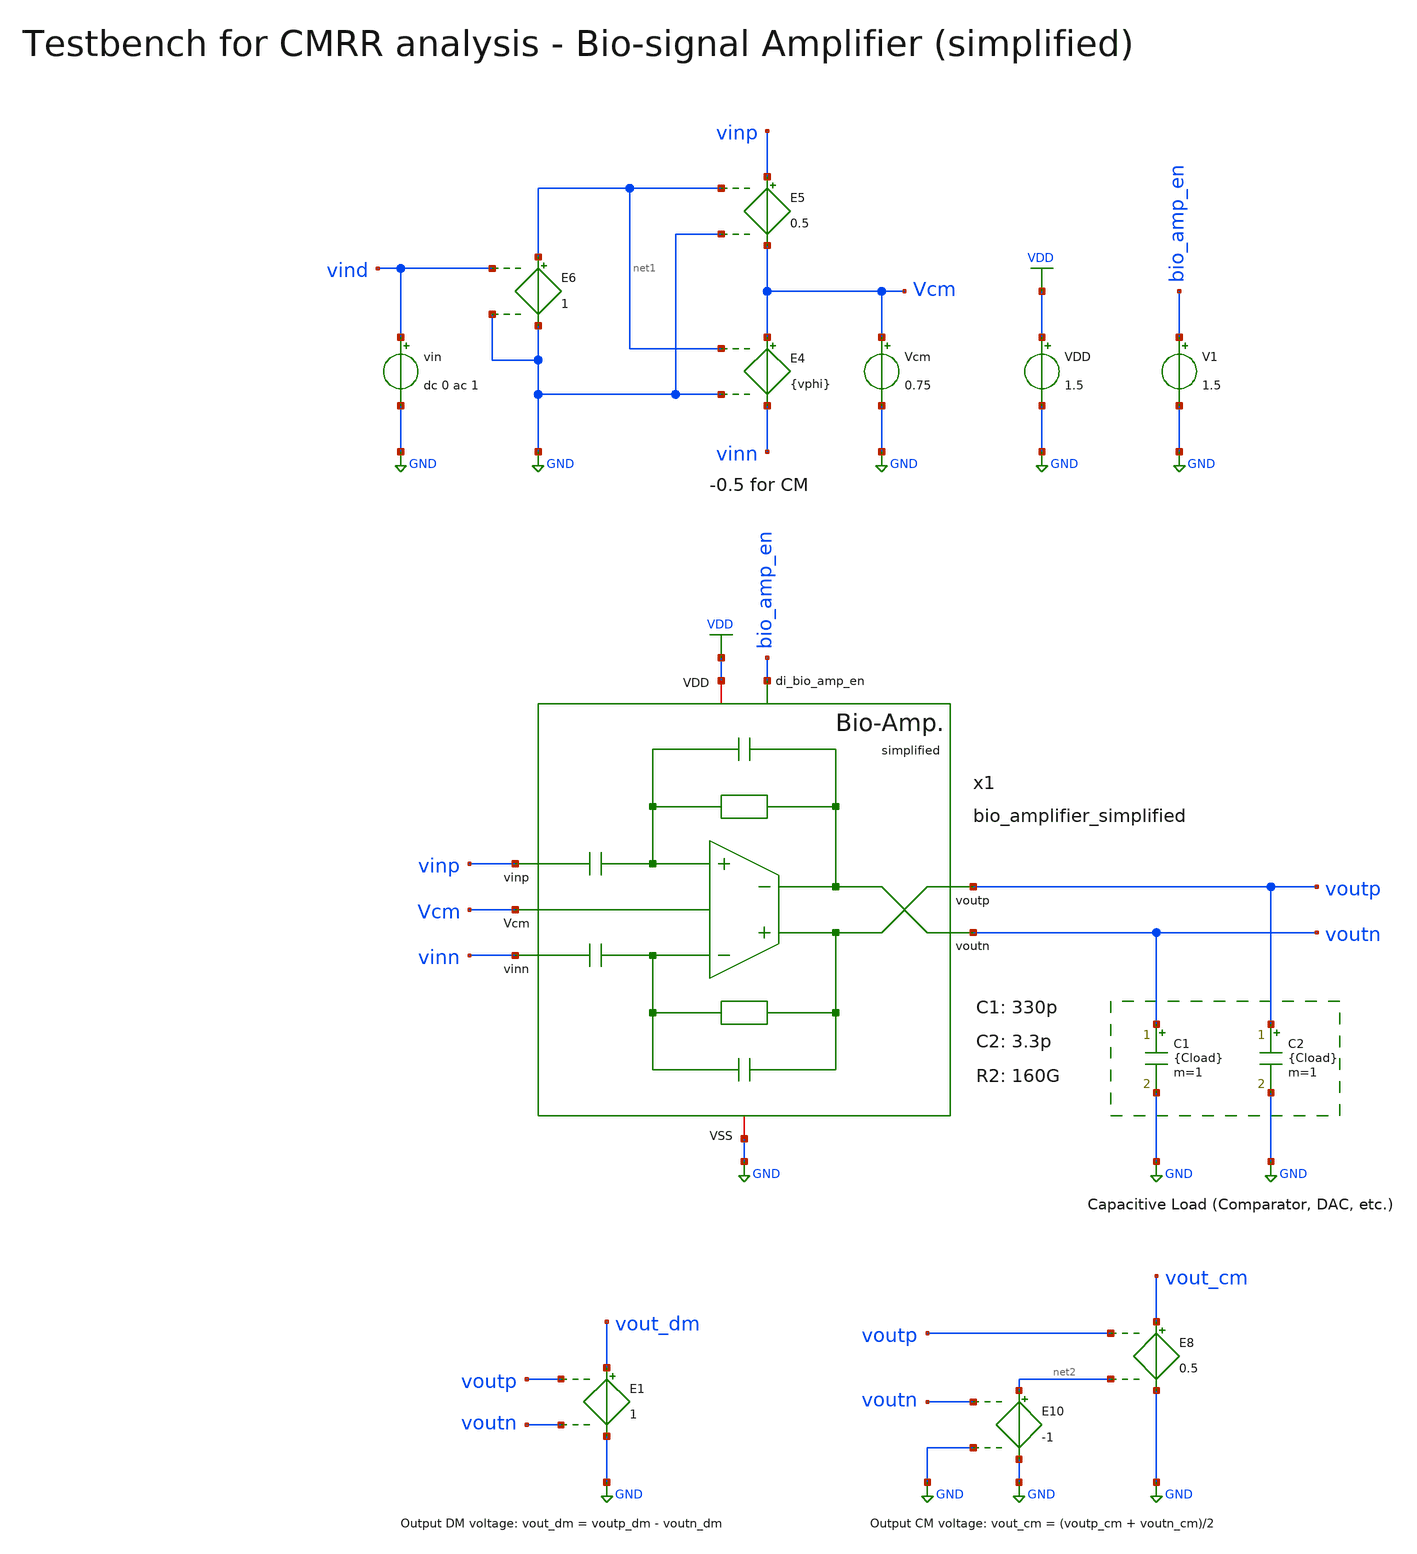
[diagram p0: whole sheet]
** sch_path: SG13G2_ATBS-ADC-main/xschem/bio_amplifier/testbenches/bio_amplifier_simplified_tb_CMRR.sch
**.subckt bio_amplifier_simplified_tb_CMRR
VDD VDD GND 1.5
C1 voutn GND {Cload} m=1
C2 voutp GND {Cload} m=1
Vcm Vcm GND 0.75
E4 Vcm vinn net1 GND {vphi}
E5 vinp Vcm net1 GND 0.5
E6 net1 GND vind GND 1
V1 bio_amp_en GND 1.5
vin vind GND dc 0 ac 1
x1 voutp bio_amp_en vinp Vcm voutn vinn VDD GND bio_amplifier_simplified C1=330p C2=3.3p R2=160G
E1 vout_dm GND voutp voutn 1
E8 vout_cm GND voutp net2 0.5
E10 net2 GND voutn GND -1
**** begin user architecture code

.lib cornerMOSlv.lib mos_tt
.lib cornerMOShv.lib mos_tt
.lib cornerRES.lib res_typ



.param temp=27
* 227.56fF DAC
.param Cload=227.56f
.param vphi=0.5
.param f_min = 10m
.csparam f_min = f_min
.param f_max = 1G
.csparam f_max = f_max
.param fdc = 10
.csparam fdc = fdc
.options savecurrents method=gear reltol=1e-2 abstol=1e-15 gmin=1e-15 rshunt=1e12
.control

* Operating Point Analysis
optran 0 0 0 1u 1m 0
save all
op
remzerovec
write bio_amplifier_simplified_tb_CMRR.raw
set appendwrite
reset

* Differential-Mode
optran 0 0 0 1u 1m 0
save v(vout_dm) v(vind)

* AC Analysis (Differential-Mode)
ac dec 101 $&f_min $&f_max
remzerovec
write bio_amplifier_simplified_tb_CMRR.raw

* Plotting Differential Mode Gain
let Adm = v(vout_dm)/v(vind)
let Adm_dB = vdb(Adm)
let Adm_arg = 180/PI*cphase(Adm)
plot Adm_dB Adm_arg ylabel 'Magnitude, Phase'

* Change to Common-Mode
alterparam vphi = -0.5
reset

optran 0 0 0 1u 1m 0
save v(vout_cm) v(vind)

* AC Analysis (Common-Mode)
ac dec 101 $&f_min $&f_max
remzerovec
write bio_amplifier_simplified_tb_CMRR.raw

* Plotting Common Mode Gain
let Acm = v(vout_cm)/v(vind)
let Acm_dB = vdb(Acm)
let Acm_arg = 180/PI*cphase(Acm)
plot Acm_dB Acm_arg ylabel 'Magnitude, Phase'

* Plotting Common Mode Rejection Ratio
* let CMRR = v(ac1.vout_dm)/v(ac2.vout_cm)
let CMRR = v(ac1.Adm)/v(ac2.Acm)
let CMRR_dB = vdb(CMRR)
* let CMRR_dB = ac1.Adm_dB - ac2.Acm_dB
let CMRR_arg = 180/PI*cphase(CMRR)
plot CMRR_dB CMRR_arg ylabel 'Magnitude, Phase'

* Measurements
meas ac CMRRdc_dB find CMRR_dB when frequency = fdc
print CMRRdc_dB

* Write Data
set wr_vecnames
set wr_singlescale
wrdata
+ /foss/designs/SG13G2_ATBS-ADC-main/python/plot_simulations/data/bio_amplifier_simplified_tb_CMRR.txt v(CMRR_dB) v(CMRR_arg)

*quit
.endc


**** end user architecture code
**.ends
.GLOBAL GND
.GLOBAL VDD
.end
